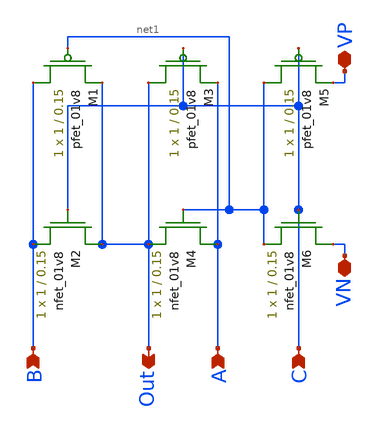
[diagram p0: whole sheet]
** sch_path: analog/amux.sch
**.subckt amux VN VP C A B Out
*.iopin VN
*.iopin VP
*.ipin C
*.ipin A
*.ipin B
*.opin Out
XM1 B net1 Out VDD sky130_fd_pr__pfet_01v8 L=0.15 W=1 nf=1 ad='int((nf+1)/2) * W/nf * 0.29' as='int((nf+2)/2) * W/nf * 0.29'
+ pd='2*int((nf+1)/2) * (W/nf + 0.29)' ps='2*int((nf+2)/2) * (W/nf + 0.29)' nrd='0.29 / W' nrs='0.29 / W'
+ sa=0 sb=0 sd=0 mult=1 m=1
XM2 Out C B GND sky130_fd_pr__nfet_01v8 L=0.15 W=1 nf=1 ad='int((nf+1)/2) * W/nf * 0.29' as='int((nf+2)/2) * W/nf * 0.29'
+ pd='2*int((nf+1)/2) * (W/nf + 0.29)' ps='2*int((nf+2)/2) * (W/nf + 0.29)' nrd='0.29 / W' nrs='0.29 / W'
+ sa=0 sb=0 sd=0 mult=1 m=1
XM3 Out C A VDD sky130_fd_pr__pfet_01v8 L=0.15 W=1 nf=1 ad='int((nf+1)/2) * W/nf * 0.29' as='int((nf+2)/2) * W/nf * 0.29'
+ pd='2*int((nf+1)/2) * (W/nf + 0.29)' ps='2*int((nf+2)/2) * (W/nf + 0.29)' nrd='0.29 / W' nrs='0.29 / W'
+ sa=0 sb=0 sd=0 mult=1 m=1
XM4 A net1 Out GND sky130_fd_pr__nfet_01v8 L=0.15 W=1 nf=1 ad='int((nf+1)/2) * W/nf * 0.29' as='int((nf+2)/2) * W/nf * 0.29'
+ pd='2*int((nf+1)/2) * (W/nf + 0.29)' ps='2*int((nf+2)/2) * (W/nf + 0.29)' nrd='0.29 / W' nrs='0.29 / W'
+ sa=0 sb=0 sd=0 mult=1 m=1
XM5 net1 C VP VDD sky130_fd_pr__pfet_01v8 L=0.15 W=1 nf=1 ad='int((nf+1)/2) * W/nf * 0.29' as='int((nf+2)/2) * W/nf * 0.29'
+ pd='2*int((nf+1)/2) * (W/nf + 0.29)' ps='2*int((nf+2)/2) * (W/nf + 0.29)' nrd='0.29 / W' nrs='0.29 / W'
+ sa=0 sb=0 sd=0 mult=1 m=1
XM6 VN C net1 GND sky130_fd_pr__nfet_01v8 L=0.15 W=1 nf=1 ad='int((nf+1)/2) * W/nf * 0.29' as='int((nf+2)/2) * W/nf * 0.29'
+ pd='2*int((nf+1)/2) * (W/nf + 0.29)' ps='2*int((nf+2)/2) * (W/nf + 0.29)' nrd='0.29 / W' nrs='0.29 / W'
+ sa=0 sb=0 sd=0 mult=1 m=1
**.ends
.end
